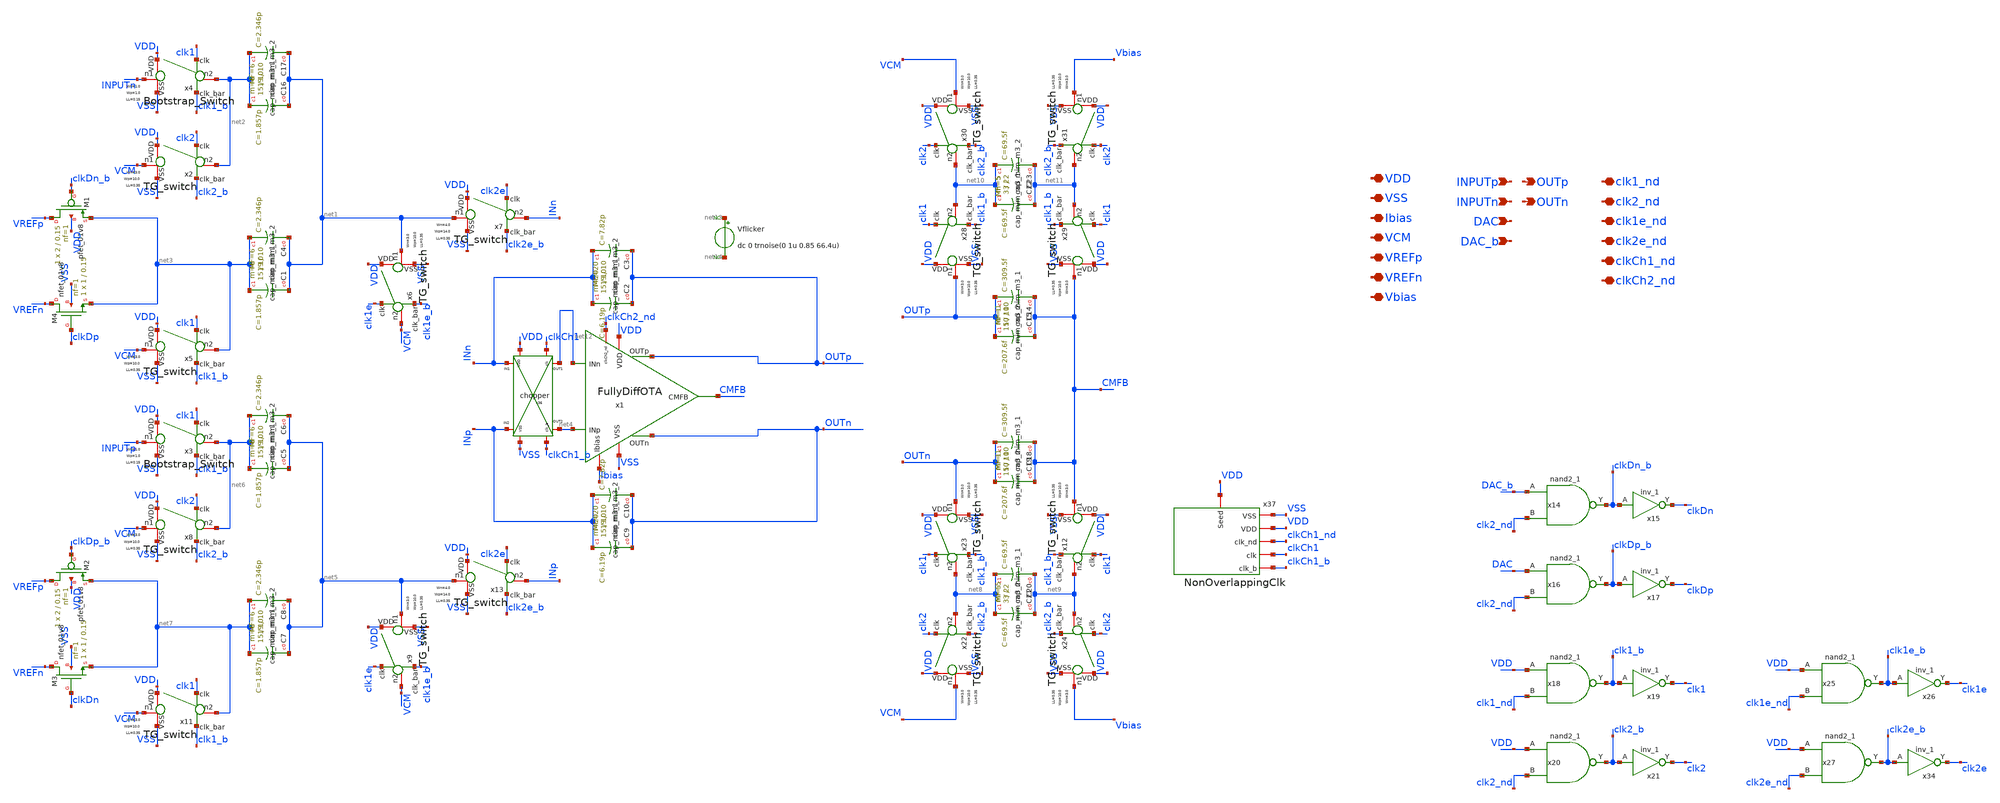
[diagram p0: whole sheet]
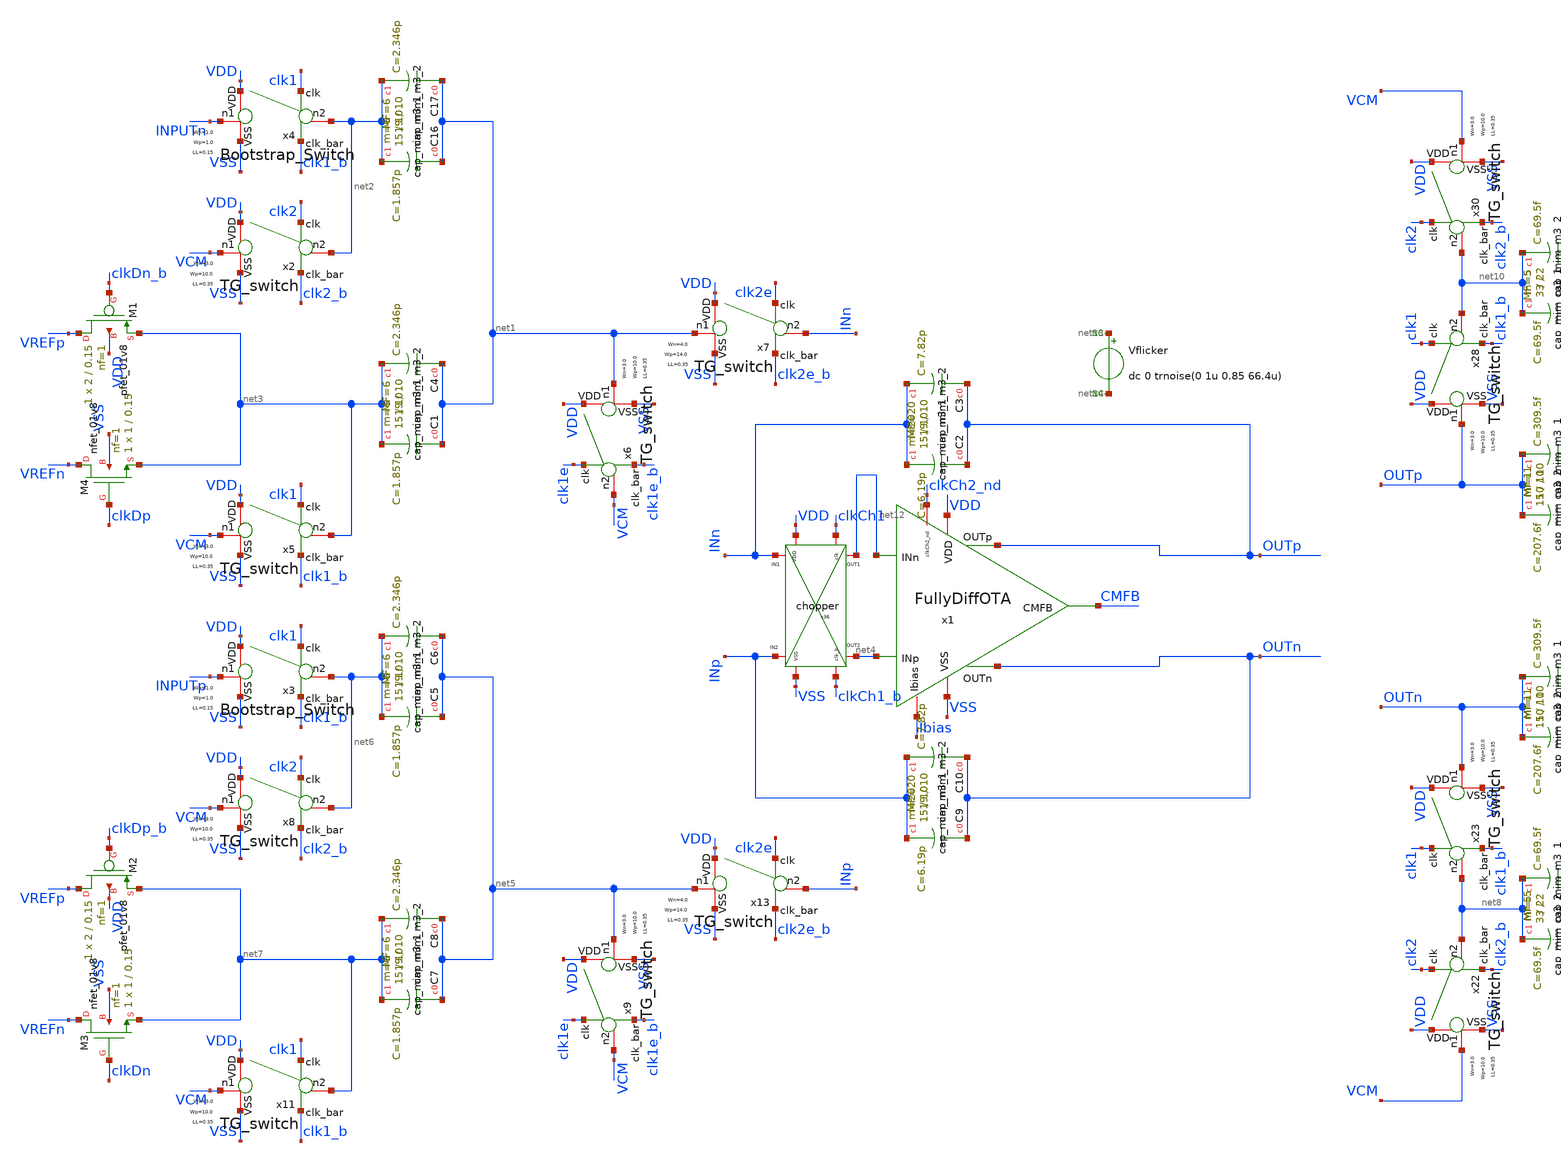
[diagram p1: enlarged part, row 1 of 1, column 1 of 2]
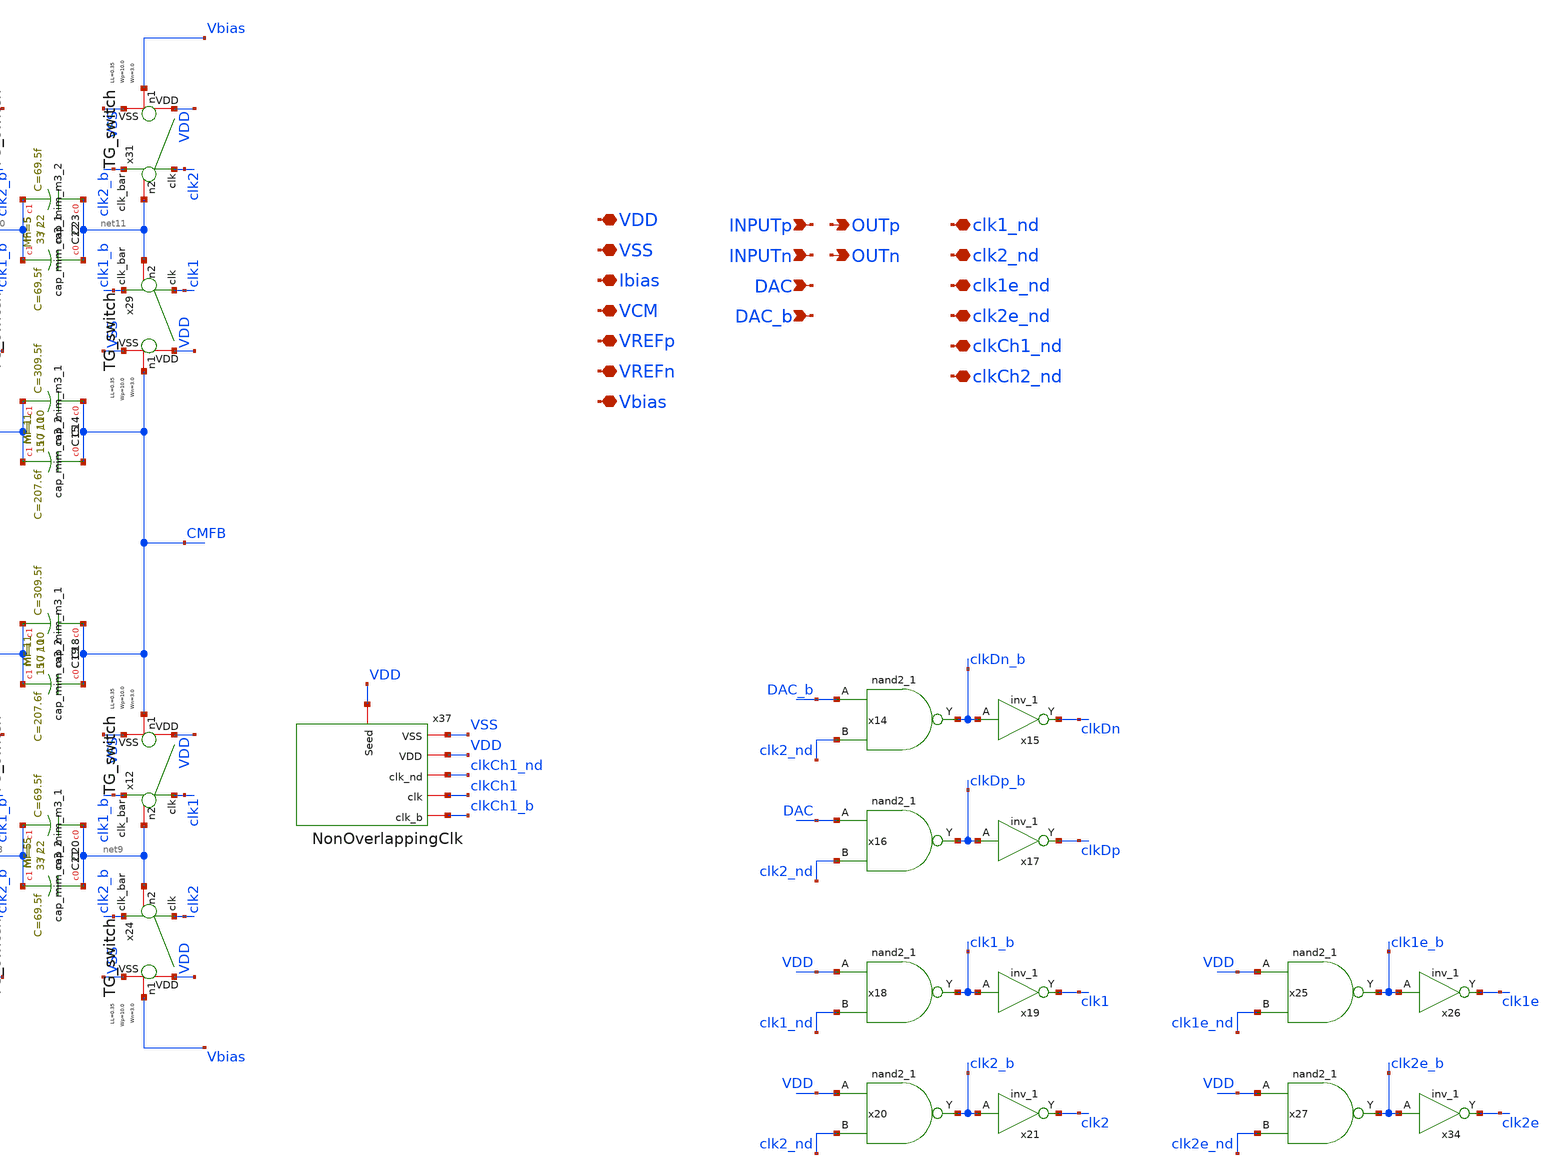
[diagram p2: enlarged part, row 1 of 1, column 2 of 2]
** sch_path: xschem/lib/Analog/SC_Integrator.sch
**.subckt SC_Integrator clk2e_nd clk1e_nd clk2_nd clk1_nd VDD VSS VCM Ibias INPUTp INPUTn VREFp
*+ VREFn Vbias DAC DAC_b OUTp OUTn clkCh1_nd clkCh2_nd
*.iopin clk2e_nd
*.iopin clk1e_nd
*.iopin clk2_nd
*.iopin clk1_nd
*.iopin VDD
*.iopin VSS
*.iopin VCM
*.iopin Ibias
*.ipin INPUTp
*.ipin INPUTn
*.iopin VREFp
*.iopin VREFn
*.iopin Vbias
*.ipin DAC
*.ipin DAC_b
*.opin OUTp
*.opin OUTn
*.iopin clkCh1_nd
*.iopin clkCh2_nd
XC16 net1 net2 sky130_fd_pr__cap_mim_m3_2 W=15 L=10 MF=6 m=6
XC17 net1 net2 sky130_fd_pr__cap_mim_m3_1 W=19 L=10 MF=6 m=6
XC2 OUTp INn sky130_fd_pr__cap_mim_m3_2 W=15 L=10 MF=20 m=20
XC3 OUTp INn sky130_fd_pr__cap_mim_m3_1 W=19 L=10 MF=20 m=20
XM2 VREFp clkDp_b net7 VDD sky130_fd_pr__pfet_01v8 L=0.15 W=2 nf=1 ad='int((1 + 1)/2) * 2 / 1 * 0.29'
+ as='int((1 + 2)/2) * 2 / 1 * 0.29' pd='2*int((1 + 1)/2) * (2 / 1 + 0.29)' ps='2*int((1 + 2)/2) * (2 / 1 + 0.29)'
+ nrd='0.29 / 2 ' nrs='0.29 / 2 ' sa=0 sb=0 sd=0 mult=1 m=1
XM1 VREFp clkDn_b net3 VDD sky130_fd_pr__pfet_01v8 L=0.15 W=2 nf=1 ad='int((1 + 1)/2) * 2 / 1 * 0.29'
+ as='int((1 + 2)/2) * 2 / 1 * 0.29' pd='2*int((1 + 1)/2) * (2 / 1 + 0.29)' ps='2*int((1 + 2)/2) * (2 / 1 + 0.29)'
+ nrd='0.29 / 2 ' nrs='0.29 / 2 ' sa=0 sb=0 sd=0 mult=1 m=1
XM3 VREFn clkDn net7 VSS sky130_fd_pr__nfet_01v8 L=0.15 W=1 nf=1 ad='int((1 + 1)/2) * 1 / 1 * 0.29' as='int((1 + 2)/2) * 1 / 1 * 0.29'
+ pd='2*int((1 + 1)/2) * (1 / 1 + 0.29)' ps='2*int((1 + 2)/2) * (1 / 1 + 0.29)' nrd='0.29 / 1 ' nrs='0.29 / 1 '
+ sa=0 sb=0 sd=0 mult=1 m=1
XM4 VREFn clkDp net3 VSS sky130_fd_pr__nfet_01v8 L=0.15 W=1 nf=1 ad='int((1 + 1)/2) * 1 / 1 * 0.29' as='int((1 + 2)/2) * 1 / 1 * 0.29'
+ pd='2*int((1 + 1)/2) * (1 / 1 + 0.29)' ps='2*int((1 + 2)/2) * (1 / 1 + 0.29)' nrd='0.29 / 1 ' nrs='0.29 / 1 '
+ sa=0 sb=0 sd=0 mult=1 m=1
x4 clk1_b clk1 VDD VSS INPUTn net2 Bootstrap_Switch Wn=1.0 Wp=1.0 LL=0.15
x3 clk1_b clk1 VDD VSS INPUTp net6 Bootstrap_Switch Wn=1.0 Wp=1.0 LL=0.15
x6 clk1e_b clk1e VDD VSS net1 VCM TG_switch Wn=3.0 Wp=10.0 LL=0.35
x9 clk1e_b clk1e VDD VSS net5 VCM TG_switch Wn=3.0 Wp=10.0 LL=0.35
x2 clk2_b clk2 VDD VSS VCM net2 TG_switch Wn=3.0 Wp=10.0 LL=0.35
x5 clk1_b clk1 VDD VSS VCM net3 TG_switch Wn=3.0 Wp=10.0 LL=0.35
x8 clk2_b clk2 VDD VSS VCM net6 TG_switch Wn=3.0 Wp=10.0 LL=0.35
x11 clk1_b clk1 VDD VSS VCM net7 TG_switch Wn=3.0 Wp=10.0 LL=0.35
x7 clk2e_b clk2e VDD VSS net1 INn TG_switch Wn=4.0 Wp=14.0 LL=0.35
x13 clk2e_b clk2e VDD VSS net5 INp TG_switch Wn=4.0 Wp=14.0 LL=0.35
XC14 CMFB OUTp sky130_fd_pr__cap_mim_m3_2 W=15 L=10 MF=1 m=1
XC15 CMFB OUTp sky130_fd_pr__cap_mim_m3_1 W=10 L=10 MF=1 m=1
XC18 CMFB OUTn sky130_fd_pr__cap_mim_m3_2 W=15 L=10 MF=1 m=1
XC19 CMFB OUTn sky130_fd_pr__cap_mim_m3_1 W=10 L=10 MF=1 m=1
x23 clk1_b clk1 VDD VSS OUTn net8 TG_switch Wn=3.0 Wp=10.0 LL=0.35
x12 clk1_b clk1 VDD VSS CMFB net9 TG_switch Wn=3.0 Wp=10.0 LL=0.35
x22 clk2_b clk2 VDD VSS VCM net8 TG_switch Wn=3.0 Wp=10.0 LL=0.35
x24 clk2_b clk2 VDD VSS Vbias net9 TG_switch Wn=3.0 Wp=10.0 LL=0.35
XC20 net9 net8 sky130_fd_pr__cap_mim_m3_2 W=3 L=2 MF=5 m=5
XC21 net9 net8 sky130_fd_pr__cap_mim_m3_1 W=3 L=2 MF=5 m=5
x28 clk1_b clk1 VDD VSS OUTp net10 TG_switch Wn=3.0 Wp=10.0 LL=0.35
x29 clk1_b clk1 VDD VSS CMFB net11 TG_switch Wn=3.0 Wp=10.0 LL=0.35
x30 clk2_b clk2 VDD VSS VCM net10 TG_switch Wn=3.0 Wp=10.0 LL=0.35
x31 clk2_b clk2 VDD VSS Vbias net11 TG_switch Wn=3.0 Wp=10.0 LL=0.35
XC22 net11 net10 sky130_fd_pr__cap_mim_m3_2 W=3 L=2 MF=5 m=5
XC23 net11 net10 sky130_fd_pr__cap_mim_m3_1 W=3 L=2 MF=5 m=5
Vflicker net13 net14 dc 0 trnoise(0 1u 0.85 66.4u)
XC1 net1 net3 sky130_fd_pr__cap_mim_m3_2 W=15 L=10 MF=6 m=6
XC4 net1 net3 sky130_fd_pr__cap_mim_m3_1 W=19 L=10 MF=6 m=6
XC5 net5 net6 sky130_fd_pr__cap_mim_m3_2 W=15 L=10 MF=6 m=6
XC6 net5 net6 sky130_fd_pr__cap_mim_m3_1 W=19 L=10 MF=6 m=6
XC7 net5 net7 sky130_fd_pr__cap_mim_m3_2 W=15 L=10 MF=6 m=6
XC8 net5 net7 sky130_fd_pr__cap_mim_m3_1 W=19 L=10 MF=6 m=6
XC9 OUTn INp sky130_fd_pr__cap_mim_m3_2 W=15 L=10 MF=20 m=20
XC10 OUTn INp sky130_fd_pr__cap_mim_m3_1 W=19 L=10 MF=20 m=20
x36 clkCh1 VDD clkCh1_b VSS net12 INn net4 INp chopper
x37 VSS VDD clkCh1_nd clkCh1 clkCh1_b VDD NonOverlappingClk
x14 DAC_b clk2_nd VSS VSS VDD VDD clkDn_b sky130_fd_sc_hd__nand2_1
x15 clkDn_b VSS VSS VDD VDD clkDn sky130_fd_sc_hd__inv_1
x16 DAC clk2_nd VSS VSS VDD VDD clkDp_b sky130_fd_sc_hd__nand2_1
x17 clkDp_b VSS VSS VDD VDD clkDp sky130_fd_sc_hd__inv_1
x18 VDD clk1_nd VSS VSS VDD VDD clk1_b sky130_fd_sc_hd__nand2_1
x19 clk1_b VSS VSS VDD VDD clk1 sky130_fd_sc_hd__inv_1
x20 VDD clk2_nd VSS VSS VDD VDD clk2_b sky130_fd_sc_hd__nand2_1
x21 clk2_b VSS VSS VDD VDD clk2 sky130_fd_sc_hd__inv_1
x25 VDD clk1e_nd VSS VSS VDD VDD clk1e_b sky130_fd_sc_hd__nand2_1
x26 clk1e_b VSS VSS VDD VDD clk1e sky130_fd_sc_hd__inv_1
x27 VDD clk2e_nd VSS VSS VDD VDD clk2e_b sky130_fd_sc_hd__nand2_1
x34 clk2e_b VSS VSS VDD VDD clk2e sky130_fd_sc_hd__inv_1
x1 VDD Ibias net12 OUTp OUTn net4 VSS CMFB clkCh2_nd FullyDiffOTA
* noconn #net13
* noconn #net14
**.ends
.end
